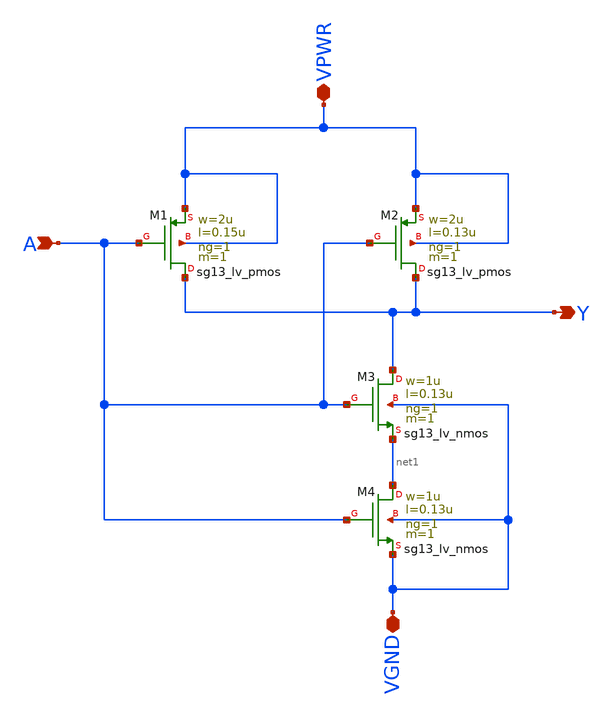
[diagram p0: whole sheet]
** sch_path: Type-II PLL-based Clock Multiplier in 130nm Bi-CMOS Technology/xschem/t2_vco_nand_inverter.sch
**.subckt t2_vco_nand_inverter VPWR VGND A Y
*.iopin VPWR
*.iopin VGND
*.ipin A
*.opin Y
XM1 Y A VPWR VPWR sg13_lv_pmos w=2u l=0.15u ng=1 m=1 mm_ok=1
XM2 Y A VPWR VPWR sg13_lv_pmos w=2u l=0.13u ng=1 m=1 mm_ok=1
XM3 Y A net1 VGND sg13_lv_nmos w=1u l=0.13u ng=1 m=1 mm_ok=1
XM4 net1 A VGND VGND sg13_lv_nmos w=1u l=0.13u ng=1 m=1 mm_ok=1
**.ends
.end
